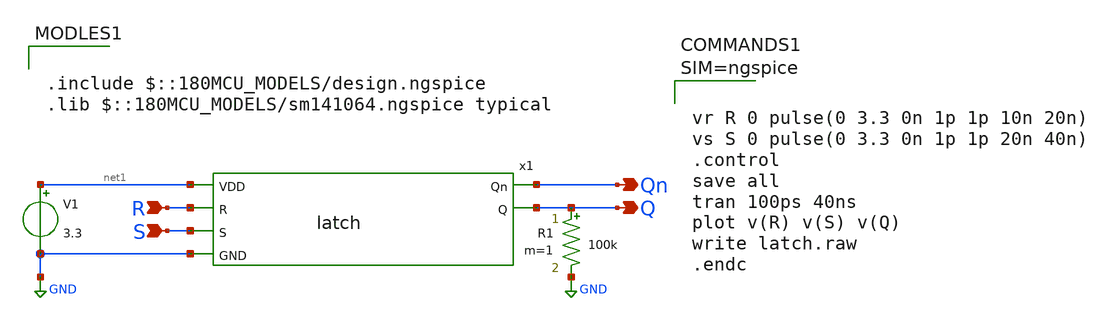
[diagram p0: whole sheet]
** sch_path: review/0407/latch/latch_test.sch
**.subckt latch_test Q R S Qn
*.opin Q
*.ipin R
*.ipin S
*.opin Qn
x1 net1 Qn Q R S GND latch
V1 net1 GND 3.3
R1 Q GND 100k m=1
**** begin user architecture code

.include $::180MCU_MODELS/design.ngspice
.lib $::180MCU_MODELS/sm141064.ngspice typical




vr R 0 pulse(0 3.3 0n 1p 1p 10n 20n)
vs S 0 pulse(0 3.3 0n 1p 1p 20n 40n)
.control
save all
tran 100ps 40ns
plot v(R) v(S) v(Q)
write latch.raw
.endc



**** end user architecture code
**.ends
.GLOBAL GND
.end
